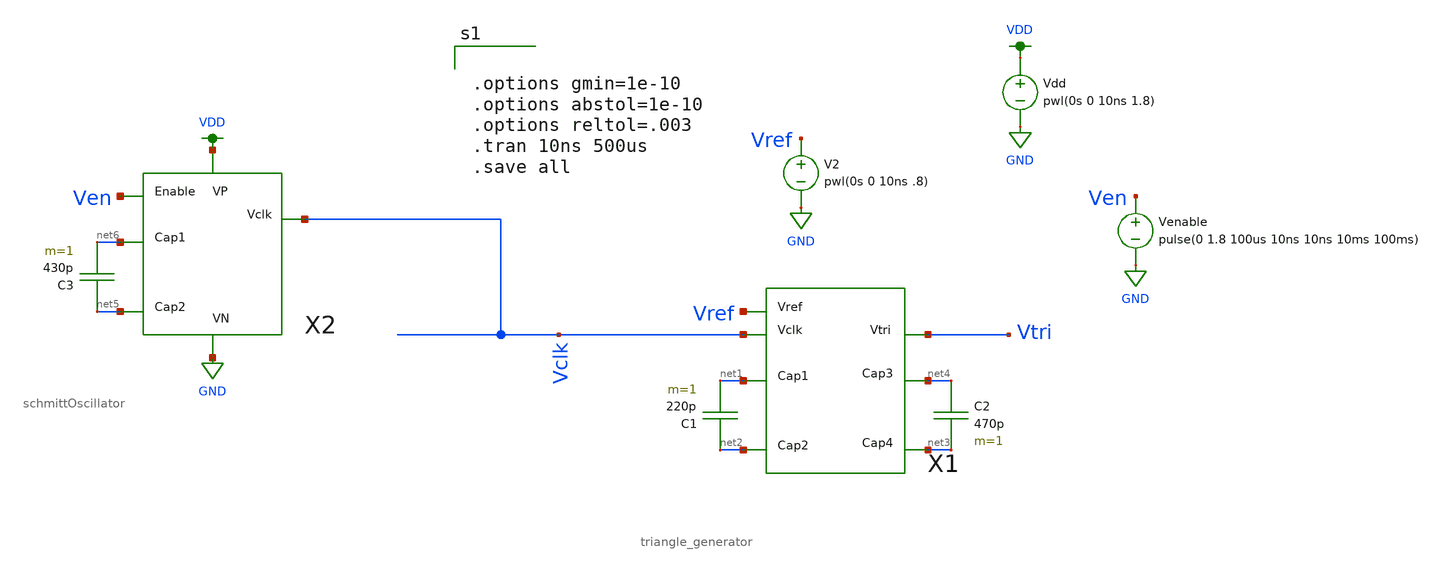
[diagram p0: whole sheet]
** sch_path: schematics/triangle_generator_testbench.sch
**.subckt triangle_generator_testbench
Vdd VDD GND pwl(0s 0 10ns 1.8)
V2 Vref GND pwl(0s 0 10ns .8)
X1 Vtri Vref net1 Vclk net2 net4 net3 triangle_generator
C1 net2 net1 220p m=1
C2 net4 net3 470p m=1
X2 Ven net6 net5 VDD GND Vclk schmittOscillator
C3 net5 net6 430p m=1
Venable Ven GND pulse(0 1.8 100us 10ns 10ns 10ms 100ms)
**** begin user architecture code


.options gmin=1e-10
.options abstol=1e-10
.options reltol=.003
.tran 10ns 500us
.save all


.option wnflag=1
.param MC_SWITCH=0.0
.lib ~/skywater/skywater-pdk/libraries/sky130_fd_pr_ngspice/latest/models/sky130.lib.spice tt

**** end user architecture code
**.ends
.GLOBAL GND
.GLOBAL VDD
.end
